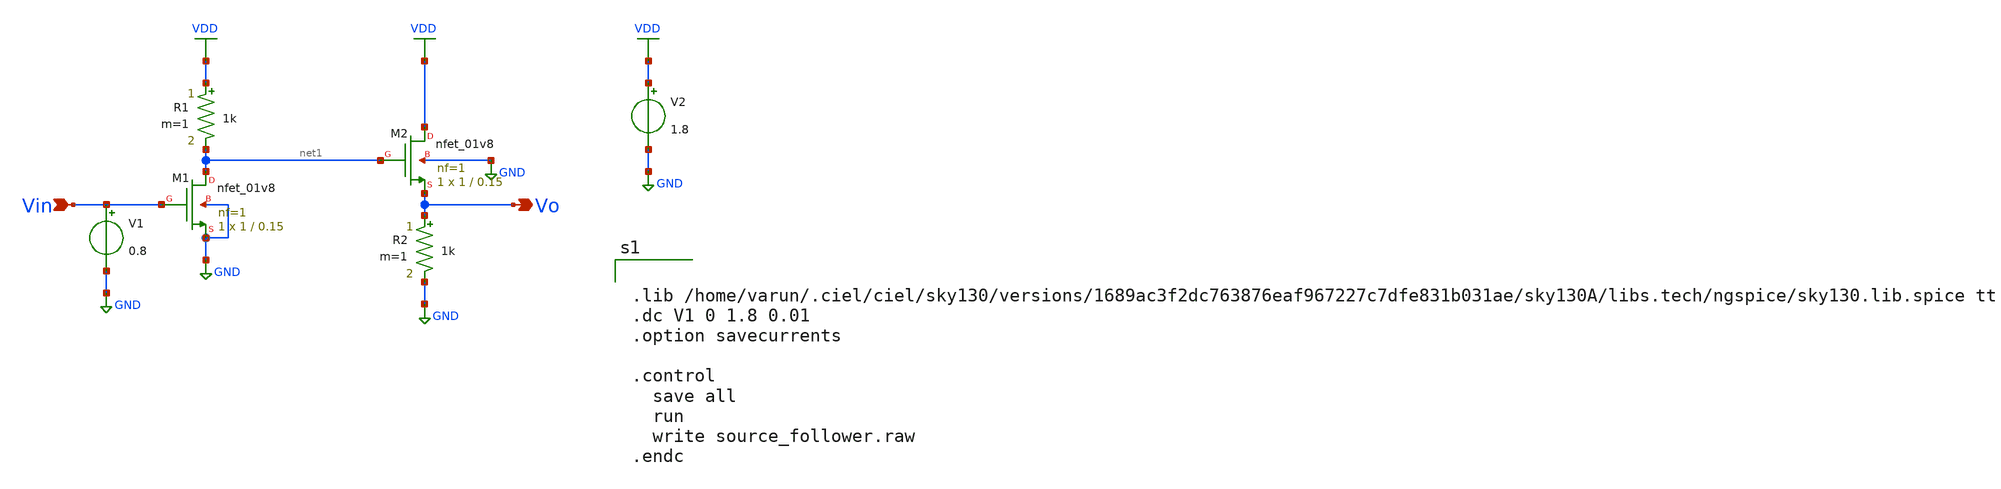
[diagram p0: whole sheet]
** sch_path: SINGLE_STAGE_AMP/SOURCE_FOLLOWER/source_follower.sch
**.subckt source_follower Vin Vo
*.ipin Vin
*.opin Vo
R1 VDD net1 1k m=1
R2 Vo GND 1k m=1
V1 Vin GND 0.8
V2 VDD GND 1.8
XM1 net1 Vin GND GND sky130_fd_pr__nfet_01v8 L=0.15 W=1 nf=1 ad='int((nf+1)/2) * W/nf * 0.29' as='int((nf+2)/2) * W/nf * 0.29'
+ pd='2*int((nf+1)/2) * (W/nf + 0.29)' ps='2*int((nf+2)/2) * (W/nf + 0.29)' nrd='0.29 / W' nrs='0.29 / W'
+ sa=0 sb=0 sd=0 mult=1 m=1
XM2 VDD net1 Vo GND sky130_fd_pr__nfet_01v8 L=0.15 W=1 nf=1 ad='int((nf+1)/2) * W/nf * 0.29' as='int((nf+2)/2) * W/nf * 0.29'
+ pd='2*int((nf+1)/2) * (W/nf + 0.29)' ps='2*int((nf+2)/2) * (W/nf + 0.29)' nrd='0.29 / W' nrs='0.29 / W'
+ sa=0 sb=0 sd=0 mult=1 m=1
**** begin user architecture code


.lib /home/varun/.ciel/ciel/sky130/versions/1689ac3f2dc763876eaf967227c7dfe831b031ae/sky130A/libs.tech/ngspice/sky130.lib.spice tt
.dc V1 0 1.8 0.01
.option savecurrents

.control
  save all
  run
  write source_follower.raw
.endc


**** end user architecture code
**.ends
.GLOBAL VDD
.GLOBAL GND
.end
